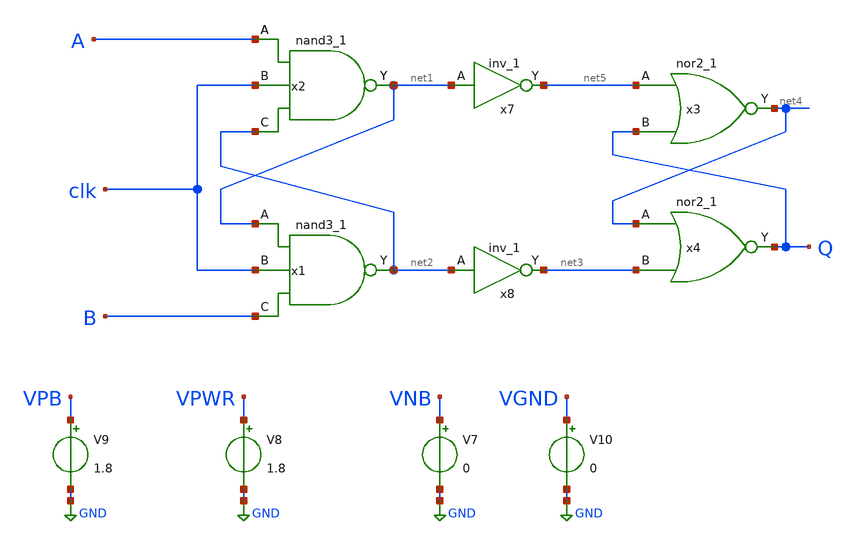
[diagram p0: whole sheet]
** sch_path: cmp/nandcmp.sch
**.subckt nandcmp
x1 net1 clk B VGND VNB VPB VPWR net2 sky130_fd_sc_hd__nand3_1
x2 A clk net2 VGND VNB VPB VPWR net1 sky130_fd_sc_hd__nand3_1
x7 net1 VGND VNB VPB VPWR net5 sky130_fd_sc_hd__inv_1
x8 net2 VGND VNB VPB VPWR net3 sky130_fd_sc_hd__inv_1
x3 net5 Q VGND VNB VPB VPWR net4 sky130_fd_sc_hd__nor2_1
x4 net4 net3 VGND VNB VPB VPWR Q sky130_fd_sc_hd__nor2_1
V7 VNB GND 0
V8 VPWR GND 1.8
V9 VPB GND 1.8
V10 VGND GND 0
**.ends
.GLOBAL GND
.end
